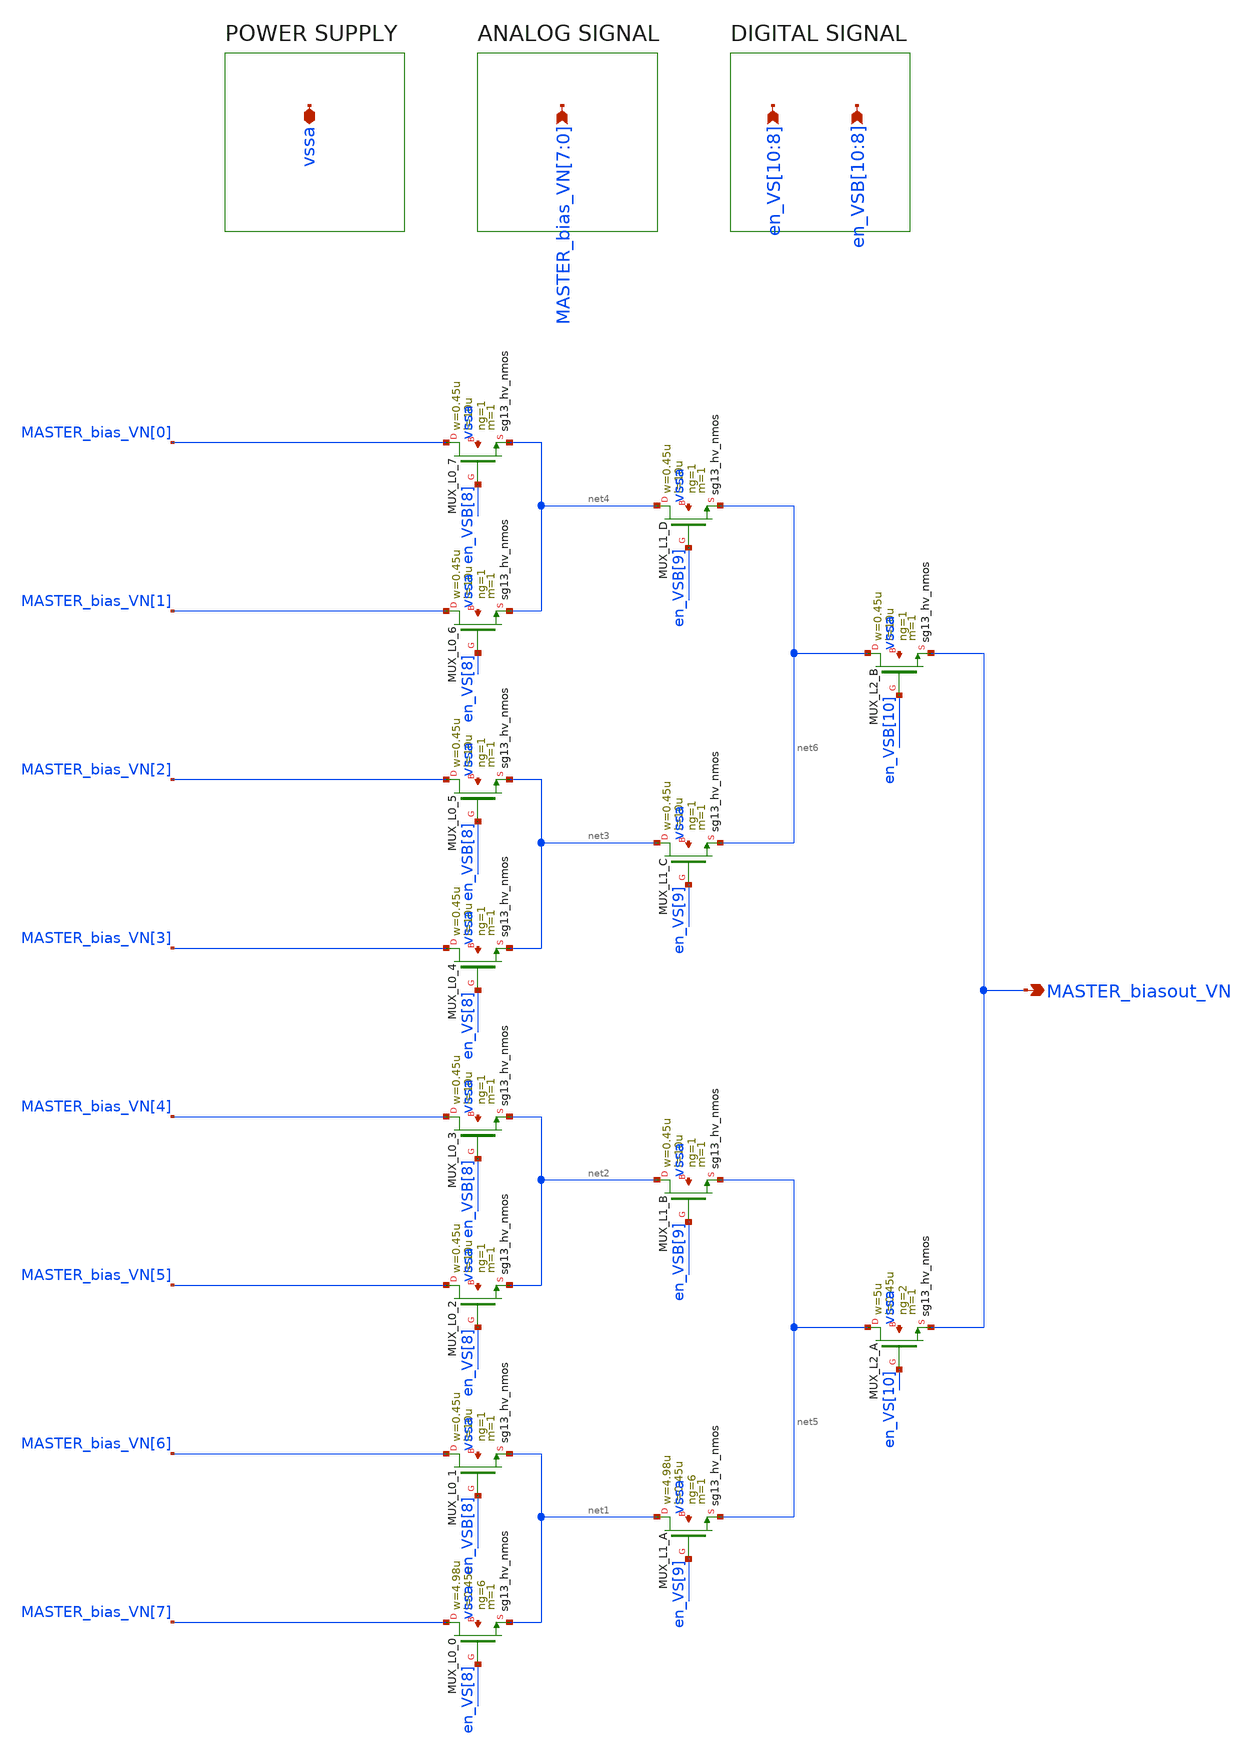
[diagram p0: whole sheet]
** sch_path: SelMUX.sch
**.subckt SelMUX
*+ MASTER_bias_VN[7],MASTER_bias_VN[6],MASTER_bias_VN[5],MASTER_bias_VN[4],MASTER_bias_VN[3],MASTER_bias_VN[2],MASTER_bias_VN[1],MASTER_bias_VN[0] MASTER_biasout_VN en_VS[10],en_VS[9],en_VS[8] en_VSB[10],en_VSB[9],en_VSB[8] vssa
*.ipin
*+ MASTER_bias_VN[7],MASTER_bias_VN[6],MASTER_bias_VN[5],MASTER_bias_VN[4],MASTER_bias_VN[3],MASTER_bias_VN[2],MASTER_bias_VN[1],MASTER_bias_VN[0]
*.opin MASTER_biasout_VN
*.ipin en_VS[10],en_VS[9],en_VS[8]
*.ipin en_VSB[10],en_VSB[9],en_VSB[8]
*.iopin vssa
XMUX_L0_0 MASTER_bias_VN[7] en_VS[8] net1 vssa sg13_hv_nmos w=4.98u l=0.45u ng=6 m=1 mm_ok=1
XMUX_L0_1 MASTER_bias_VN[6] en_VSB[8] net1 vssa sg13_hv_nmos w=0.45u l=10u ng=1 m=1 mm_ok=1
XMUX_L0_2 MASTER_bias_VN[5] en_VS[8] net2 vssa sg13_hv_nmos w=0.45u l=10u ng=1 m=1 mm_ok=1
XMUX_L0_3 MASTER_bias_VN[4] en_VSB[8] net2 vssa sg13_hv_nmos w=0.45u l=10u ng=1 m=1 mm_ok=1
XMUX_L0_4 MASTER_bias_VN[3] en_VS[8] net3 vssa sg13_hv_nmos w=0.45u l=10u ng=1 m=1 mm_ok=1
XMUX_L0_5 MASTER_bias_VN[2] en_VSB[8] net3 vssa sg13_hv_nmos w=0.45u l=10u ng=1 m=1 mm_ok=1
XMUX_L0_6 MASTER_bias_VN[1] en_VS[8] net4 vssa sg13_hv_nmos w=0.45u l=10u ng=1 m=1 mm_ok=1
XMUX_L0_7 MASTER_bias_VN[0] en_VSB[8] net4 vssa sg13_hv_nmos w=0.45u l=10u ng=1 m=1 mm_ok=1
XMUX_L1_A net1 en_VS[9] net5 vssa sg13_hv_nmos w=4.98u l=0.45u ng=6 m=1 mm_ok=1
XMUX_L1_B net2 en_VSB[9] net5 vssa sg13_hv_nmos w=0.45u l=10u ng=1 m=1 mm_ok=1
XMUX_L1_C net3 en_VS[9] net6 vssa sg13_hv_nmos w=0.45u l=10u ng=1 m=1 mm_ok=1
XMUX_L1_D net4 en_VSB[9] net6 vssa sg13_hv_nmos w=0.45u l=10u ng=1 m=1 mm_ok=1
XMUX_L2_A net5 en_VS[10] MASTER_biasout_VN vssa sg13_hv_nmos w=5u l=0.45u ng=2 m=1 mm_ok=1
XMUX_L2_B net6 en_VSB[10] MASTER_biasout_VN vssa sg13_hv_nmos w=0.45u l=10u ng=1 m=1 mm_ok=1
**.ends
.end
